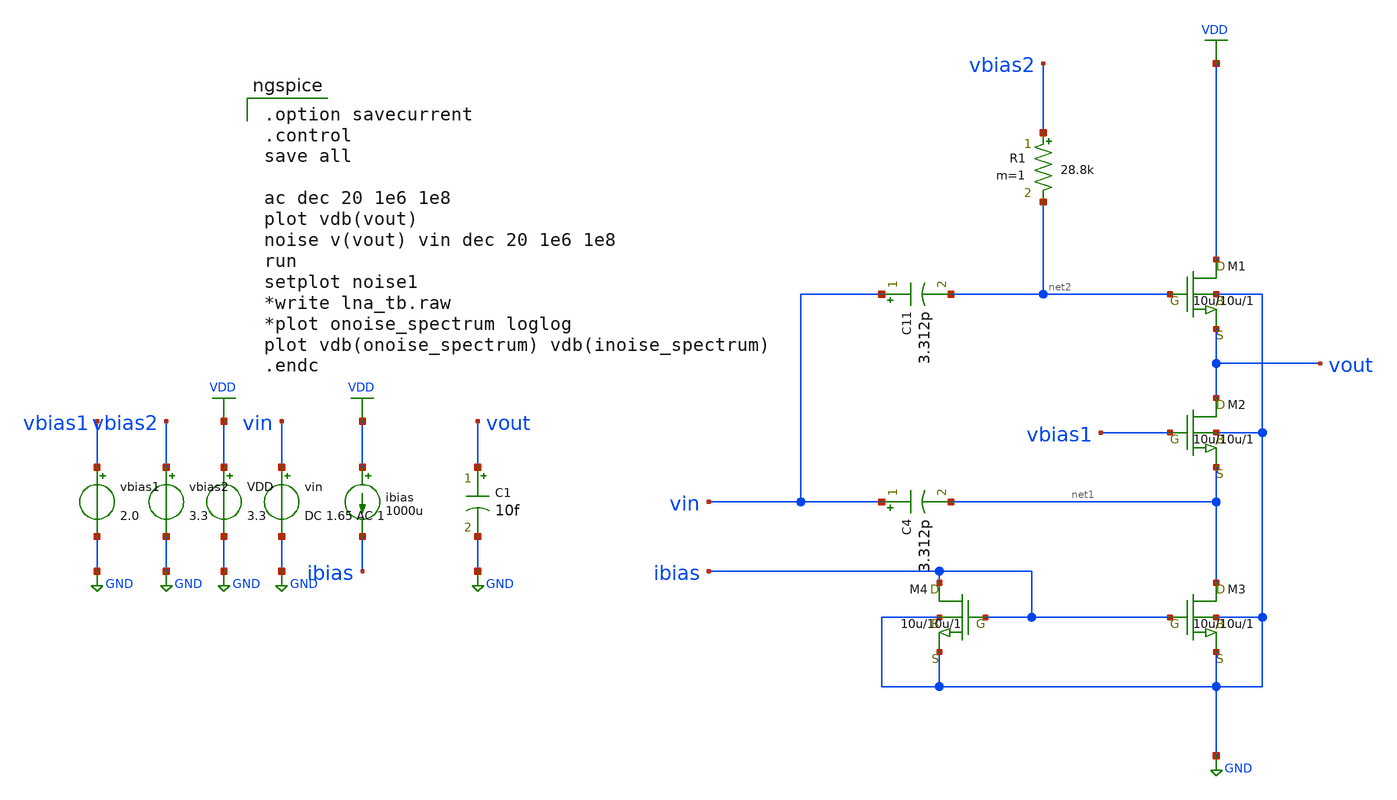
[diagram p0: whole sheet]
** sch_path: LNA/lna_tb.sch
**.subckt lna_tb
vbias1 vbias1 GND 2.0
vbias2 vbias2 GND 3.3
VDD VDD GND 3.3
vin vin GND DC 1.65 AC 1
ibias VDD ibias 1000u
M1 VDD net2 vout GND nch w=10u l=10u as=0 ps=0 ad=0 pd=0 m=1
M2 vout vbias1 net1 GND nch w=10u l=10u as=0 ps=0 ad=0 pd=0 m=1
M3 net1 ibias GND GND nch w=10u l=10u as=0 ps=0 ad=0 pd=0 m=1
M4 ibias ibias GND GND nch w=10u l=10u as=0 ps=0 ad=0 pd=0 m=1
C4 vin net1 3.312p m=1
R1 vbias2 net2 28.8k m=1
C1 vout GND 10f m=1
C11 vin net2 3.312p m=1
**** begin user architecture code
 .include $::LIB/SOI_CMOS

.option savecurrent
.control
save all

ac dec 20 1e6 1e8
plot vdb(vout)
noise v(vout) vin dec 20 1e6 1e8
run
setplot noise1
*write lna_tb.raw
*plot onoise_spectrum loglog
plot vdb(onoise_spectrum) vdb(inoise_spectrum)
.endc

**** end user architecture code
**.ends
.GLOBAL VDD
.GLOBAL GND
.end
